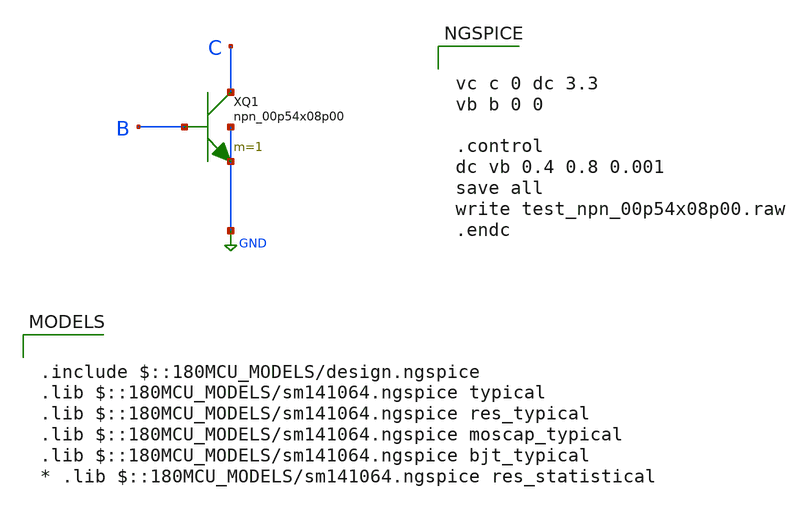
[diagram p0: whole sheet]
** sch_path: gf180mcuD/xschem_libs/gf180mcu_tests/test_npn_00p54x08p00/schematic/test_npn_00p54x08p00.sch
* Copyright 2022 GlobalFoundries PDK Authors
* Licensed under the Apache License, Version 2.0 (the "License");
* you may not use this file except in compliance with the License.
* You may obtain a copy of the License at
* https://www.apache.org/licenses/LICENSE-2.0
* Unless required by applicable law or agreed to in writing, software
* distributed under the License is distributed on an "AS IS" BASIS,
* WITHOUT WARRANTIES OR CONDITIONS OF ANY KIND, either express or implied.
* See the License for the specific language governing permissions and
* limitations under the License.
**.subckt test_npn_00p54x08p00
XQ1 C B GND GND npn_00p54x08p00 m=1
**** begin user architecture code

.include $::180MCU_MODELS/design.ngspice
.lib $::180MCU_MODELS/sm141064.ngspice typical
.lib $::180MCU_MODELS/sm141064.ngspice res_typical
.lib $::180MCU_MODELS/sm141064.ngspice moscap_typical
.lib $::180MCU_MODELS/sm141064.ngspice bjt_typical
* .lib $::180MCU_MODELS/sm141064.ngspice res_statistical



vc c 0 dc 3.3
vb b 0 0

.control
dc vb 0.4 0.8 0.001
save all
write test_npn_00p54x08p00.raw
.endc


**** end user architecture code
**.ends
.GLOBAL GND
.end
